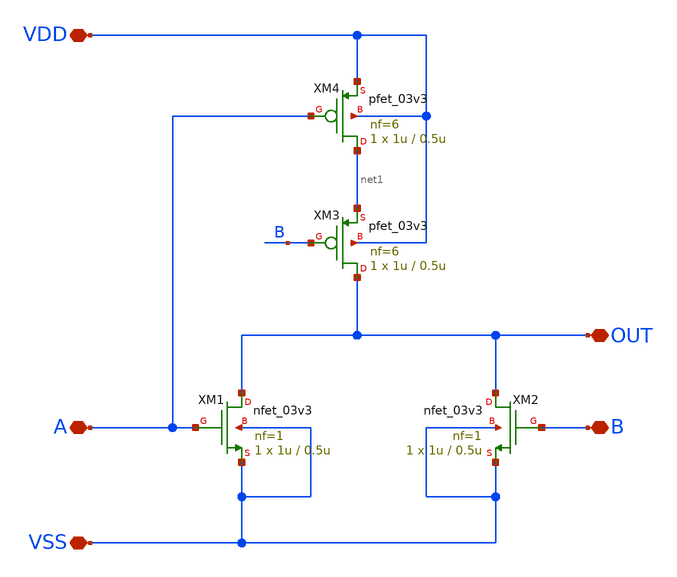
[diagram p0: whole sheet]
** sch_path: designs/libs/xp_core_analog/asc_NOR/asc_NOR.sch
**.subckt asc_NOR VDD VSS B A OUT
*.iopin VDD
*.iopin VSS
*.iopin B
*.iopin A
*.iopin OUT
XM1 OUT A VSS VSS nfet_03v3 L=0.5u W=1u nf=1 ad='int((nf+1)/2) * W/nf * 0.18u' as='int((nf+2)/2) * W/nf * 0.18u'
+ pd='2*int((nf+1)/2) * (W/nf + 0.18u)' ps='2*int((nf+2)/2) * (W/nf + 0.18u)' nrd='0.18u / W' nrs='0.18u / W'
+ sa=0 sb=0 sd=0 m=1
XM2 OUT B VSS VSS nfet_03v3 L=0.5u W=1u nf=1 ad='int((nf+1)/2) * W/nf * 0.18u' as='int((nf+2)/2) * W/nf * 0.18u'
+ pd='2*int((nf+1)/2) * (W/nf + 0.18u)' ps='2*int((nf+2)/2) * (W/nf + 0.18u)' nrd='0.18u / W' nrs='0.18u / W'
+ sa=0 sb=0 sd=0 m=1
XM3 OUT B net1 VDD pfet_03v3 L=0.5u W=1u nf=6 ad='int((nf+1)/2) * W/nf * 0.18u' as='int((nf+2)/2) * W/nf * 0.18u'
+ pd='2*int((nf+1)/2) * (W/nf + 0.18u)' ps='2*int((nf+2)/2) * (W/nf + 0.18u)' nrd='0.18u / W' nrs='0.18u / W'
+ sa=0 sb=0 sd=0 m=1
XM4 net1 A VDD VDD pfet_03v3 L=0.5u W=1u nf=6 ad='int((nf+1)/2) * W/nf * 0.18u' as='int((nf+2)/2) * W/nf * 0.18u'
+ pd='2*int((nf+1)/2) * (W/nf + 0.18u)' ps='2*int((nf+2)/2) * (W/nf + 0.18u)' nrd='0.18u / W' nrs='0.18u / W'
+ sa=0 sb=0 sd=0 m=1
**.ends
.end
